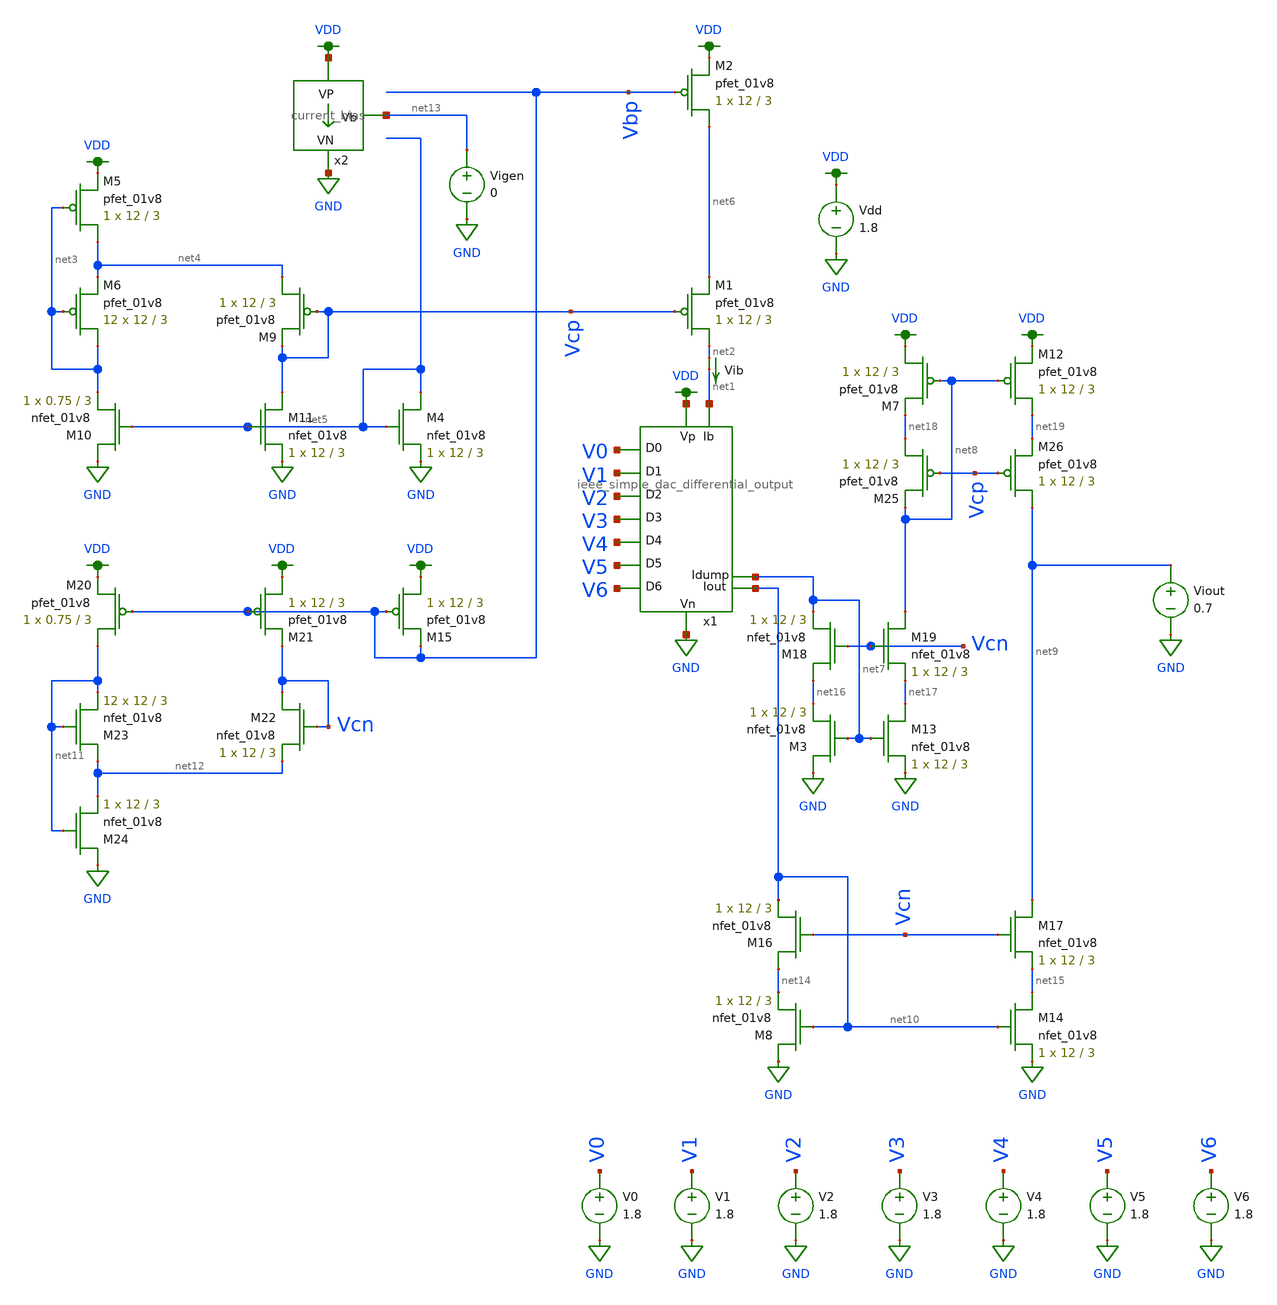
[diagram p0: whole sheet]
** sch_path: schematics/ieee DAC/ieee_DAC_mc_simulation_3.sch
**.subckt ieee_DAC_mc_simulation_3
Vdd VDD GND 1.8
V1 V1 GND 1.8
V2 V2 GND 1.8
V3 V3 GND 1.8
V4 V4 GND 1.8
V5 V5 GND 1.8
V6 V6 GND 1.8
V0 V0 GND 1.8
Vib net2 net1 0
.save i(vib)
XM1 net2 Vcp net6 VDD sky130_fd_pr__pfet_01v8 L=3 W=12 nf=1 ad='int((nf+1)/2) * W/nf * 0.29' as='int((nf+2)/2) * W/nf * 0.29'
+ pd='2*int((nf+1)/2) * (W/nf + 0.29)' ps='2*int((nf+2)/2) * (W/nf + 0.29)' nrd='0.29 / W' nrs='0.29 / W'
+ sa=0 sb=0 sd=0 mult=1 m=1
XM5 net4 net3 VDD VDD sky130_fd_pr__pfet_01v8 L=3 W=12 nf=1 ad='int((nf+1)/2) * W/nf * 0.29' as='int((nf+2)/2) * W/nf * 0.29'
+ pd='2*int((nf+1)/2) * (W/nf + 0.29)' ps='2*int((nf+2)/2) * (W/nf + 0.29)' nrd='0.29 / W' nrs='0.29 / W'
+ sa=0 sb=0 sd=0 mult=1 m=1
XM6 net3 net3 net4 VDD sky130_fd_pr__pfet_01v8 L=3 W=12 nf=1 ad='int((nf+1)/2) * W/nf * 0.29' as='int((nf+2)/2) * W/nf * 0.29'
+ pd='2*int((nf+1)/2) * (W/nf + 0.29)' ps='2*int((nf+2)/2) * (W/nf + 0.29)' nrd='0.29 / W' nrs='0.29 / W'
+ sa=0 sb=0 sd=0 mult=12 m=12
XM9 net4 Vcp Vcp VDD sky130_fd_pr__pfet_01v8 L=3 W=12 nf=1 ad='int((nf+1)/2) * W/nf * 0.29' as='int((nf+2)/2) * W/nf * 0.29'
+ pd='2*int((nf+1)/2) * (W/nf + 0.29)' ps='2*int((nf+2)/2) * (W/nf + 0.29)' nrd='0.29 / W' nrs='0.29 / W'
+ sa=0 sb=0 sd=0 mult=1 m=1
XM10 GND net5 net3 GND sky130_fd_pr__nfet_01v8 L=3 W=0.75 nf=1 ad='int((nf+1)/2) * W/nf * 0.29' as='int((nf+2)/2) * W/nf * 0.29'
+ pd='2*int((nf+1)/2) * (W/nf + 0.29)' ps='2*int((nf+2)/2) * (W/nf + 0.29)' nrd='0.29 / W' nrs='0.29 / W'
+ sa=0 sb=0 sd=0 mult=1 m=1
XM11 Vcp net5 GND GND sky130_fd_pr__nfet_01v8 L=3 W=12 nf=1 ad='int((nf+1)/2) * W/nf * 0.29' as='int((nf+2)/2) * W/nf * 0.29'
+ pd='2*int((nf+1)/2) * (W/nf + 0.29)' ps='2*int((nf+2)/2) * (W/nf + 0.29)' nrd='0.29 / W' nrs='0.29 / W'
+ sa=0 sb=0 sd=0 mult=1 m=1
XM2 net6 Vbp VDD VDD sky130_fd_pr__pfet_01v8 L=3 W=12 nf=1 ad='int((nf+1)/2) * W/nf * 0.29' as='int((nf+2)/2) * W/nf * 0.29'
+ pd='2*int((nf+1)/2) * (W/nf + 0.29)' ps='2*int((nf+2)/2) * (W/nf + 0.29)' nrd='0.29 / W' nrs='0.29 / W'
+ sa=0 sb=0 sd=0 mult=1 m=1
XM4 net5 net5 GND GND sky130_fd_pr__nfet_01v8 L=3 W=12 nf=1 ad='int((nf+1)/2) * W/nf * 0.29' as='int((nf+2)/2) * W/nf * 0.29'
+ pd='2*int((nf+1)/2) * (W/nf + 0.29)' ps='2*int((nf+2)/2) * (W/nf + 0.29)' nrd='0.29 / W' nrs='0.29 / W'
+ sa=0 sb=0 sd=0 mult=1 m=1
x2 VDD net13 GND current_bias
Vigen net13 GND 0
x1 VDD net7 GND V1 V0 V2 V3 V4 V5 V6 net1 net10 ieee_simple_dac_differential_output
XM3 GND net7 net16 GND sky130_fd_pr__nfet_01v8 L=3 W=12 nf=1 ad='int((nf+1)/2) * W/nf * 0.29' as='int((nf+2)/2) * W/nf * 0.29'
+ pd='2*int((nf+1)/2) * (W/nf + 0.29)' ps='2*int((nf+2)/2) * (W/nf + 0.29)' nrd='0.29 / W' nrs='0.29 / W'
+ sa=0 sb=0 sd=0 mult=1 m=1
XM7 VDD net8 net18 VDD sky130_fd_pr__pfet_01v8 L=3 W=12 nf=1 ad='int((nf+1)/2) * W/nf * 0.29' as='int((nf+2)/2) * W/nf * 0.29'
+ pd='2*int((nf+1)/2) * (W/nf + 0.29)' ps='2*int((nf+2)/2) * (W/nf + 0.29)' nrd='0.29 / W' nrs='0.29 / W'
+ sa=0 sb=0 sd=0 mult=1 m=1
XM8 GND net10 net14 GND sky130_fd_pr__nfet_01v8 L=3 W=12 nf=1 ad='int((nf+1)/2) * W/nf * 0.29' as='int((nf+2)/2) * W/nf * 0.29'
+ pd='2*int((nf+1)/2) * (W/nf + 0.29)' ps='2*int((nf+2)/2) * (W/nf + 0.29)' nrd='0.29 / W' nrs='0.29 / W'
+ sa=0 sb=0 sd=0 mult=1 m=1
XM12 net19 net8 VDD VDD sky130_fd_pr__pfet_01v8 L=3 W=12 nf=1 ad='int((nf+1)/2) * W/nf * 0.29' as='int((nf+2)/2) * W/nf * 0.29'
+ pd='2*int((nf+1)/2) * (W/nf + 0.29)' ps='2*int((nf+2)/2) * (W/nf + 0.29)' nrd='0.29 / W' nrs='0.29 / W'
+ sa=0 sb=0 sd=0 mult=1 m=1
Viout net9 GND 0.7
XM13 net17 net7 GND GND sky130_fd_pr__nfet_01v8 L=3 W=12 nf=1 ad='int((nf+1)/2) * W/nf * 0.29' as='int((nf+2)/2) * W/nf * 0.29'
+ pd='2*int((nf+1)/2) * (W/nf + 0.29)' ps='2*int((nf+2)/2) * (W/nf + 0.29)' nrd='0.29 / W' nrs='0.29 / W'
+ sa=0 sb=0 sd=0 mult=1 m=1
XM14 net15 net10 GND GND sky130_fd_pr__nfet_01v8 L=3 W=12 nf=1 ad='int((nf+1)/2) * W/nf * 0.29' as='int((nf+2)/2) * W/nf * 0.29'
+ pd='2*int((nf+1)/2) * (W/nf + 0.29)' ps='2*int((nf+2)/2) * (W/nf + 0.29)' nrd='0.29 / W' nrs='0.29 / W'
+ sa=0 sb=0 sd=0 mult=1 m=1
XM20 net11 Vbp VDD VDD sky130_fd_pr__pfet_01v8 L=3 W=0.75 nf=1 ad='int((nf+1)/2) * W/nf * 0.29' as='int((nf+2)/2) * W/nf * 0.29'
+ pd='2*int((nf+1)/2) * (W/nf + 0.29)' ps='2*int((nf+2)/2) * (W/nf + 0.29)' nrd='0.29 / W' nrs='0.29 / W'
+ sa=0 sb=0 sd=0 mult=1 m=1
XM21 VDD Vbp Vcn VDD sky130_fd_pr__pfet_01v8 L=3 W=12 nf=1 ad='int((nf+1)/2) * W/nf * 0.29' as='int((nf+2)/2) * W/nf * 0.29'
+ pd='2*int((nf+1)/2) * (W/nf + 0.29)' ps='2*int((nf+2)/2) * (W/nf + 0.29)' nrd='0.29 / W' nrs='0.29 / W'
+ sa=0 sb=0 sd=0 mult=1 m=1
XM22 Vcn Vcn net12 GND sky130_fd_pr__nfet_01v8 L=3 W=12 nf=1 ad='int((nf+1)/2) * W/nf * 0.29' as='int((nf+2)/2) * W/nf * 0.29'
+ pd='2*int((nf+1)/2) * (W/nf + 0.29)' ps='2*int((nf+2)/2) * (W/nf + 0.29)' nrd='0.29 / W' nrs='0.29 / W'
+ sa=0 sb=0 sd=0 mult=1 m=1
XM23 net12 net11 net11 GND sky130_fd_pr__nfet_01v8 L=3 W=12 nf=1 ad='int((nf+1)/2) * W/nf * 0.29' as='int((nf+2)/2) * W/nf * 0.29'
+ pd='2*int((nf+1)/2) * (W/nf + 0.29)' ps='2*int((nf+2)/2) * (W/nf + 0.29)' nrd='0.29 / W' nrs='0.29 / W'
+ sa=0 sb=0 sd=0 mult=12 m=12
XM24 GND net11 net12 GND sky130_fd_pr__nfet_01v8 L=3 W=12 nf=1 ad='int((nf+1)/2) * W/nf * 0.29' as='int((nf+2)/2) * W/nf * 0.29'
+ pd='2*int((nf+1)/2) * (W/nf + 0.29)' ps='2*int((nf+2)/2) * (W/nf + 0.29)' nrd='0.29 / W' nrs='0.29 / W'
+ sa=0 sb=0 sd=0 mult=1 m=1
XM15 VDD Vbp Vbp VDD sky130_fd_pr__pfet_01v8 L=3 W=12 nf=1 ad='int((nf+1)/2) * W/nf * 0.29' as='int((nf+2)/2) * W/nf * 0.29'
+ pd='2*int((nf+1)/2) * (W/nf + 0.29)' ps='2*int((nf+2)/2) * (W/nf + 0.29)' nrd='0.29 / W' nrs='0.29 / W'
+ sa=0 sb=0 sd=0 mult=1 m=1
XM16 net14 Vcn net10 GND sky130_fd_pr__nfet_01v8 L=3 W=12 nf=1 ad='int((nf+1)/2) * W/nf * 0.29' as='int((nf+2)/2) * W/nf * 0.29'
+ pd='2*int((nf+1)/2) * (W/nf + 0.29)' ps='2*int((nf+2)/2) * (W/nf + 0.29)' nrd='0.29 / W' nrs='0.29 / W'
+ sa=0 sb=0 sd=0 mult=1 m=1
XM17 net9 Vcn net15 GND sky130_fd_pr__nfet_01v8 L=3 W=12 nf=1 ad='int((nf+1)/2) * W/nf * 0.29' as='int((nf+2)/2) * W/nf * 0.29'
+ pd='2*int((nf+1)/2) * (W/nf + 0.29)' ps='2*int((nf+2)/2) * (W/nf + 0.29)' nrd='0.29 / W' nrs='0.29 / W'
+ sa=0 sb=0 sd=0 mult=1 m=1
XM18 net16 Vcn net7 GND sky130_fd_pr__nfet_01v8 L=3 W=12 nf=1 ad='int((nf+1)/2) * W/nf * 0.29' as='int((nf+2)/2) * W/nf * 0.29'
+ pd='2*int((nf+1)/2) * (W/nf + 0.29)' ps='2*int((nf+2)/2) * (W/nf + 0.29)' nrd='0.29 / W' nrs='0.29 / W'
+ sa=0 sb=0 sd=0 mult=1 m=1
XM19 net8 Vcn net17 GND sky130_fd_pr__nfet_01v8 L=3 W=12 nf=1 ad='int((nf+1)/2) * W/nf * 0.29' as='int((nf+2)/2) * W/nf * 0.29'
+ pd='2*int((nf+1)/2) * (W/nf + 0.29)' ps='2*int((nf+2)/2) * (W/nf + 0.29)' nrd='0.29 / W' nrs='0.29 / W'
+ sa=0 sb=0 sd=0 mult=1 m=1
XM25 net18 Vcp net8 VDD sky130_fd_pr__pfet_01v8 L=3 W=12 nf=1 ad='int((nf+1)/2) * W/nf * 0.29' as='int((nf+2)/2) * W/nf * 0.29'
+ pd='2*int((nf+1)/2) * (W/nf + 0.29)' ps='2*int((nf+2)/2) * (W/nf + 0.29)' nrd='0.29 / W' nrs='0.29 / W'
+ sa=0 sb=0 sd=0 mult=1 m=1
XM26 net9 Vcp net19 VDD sky130_fd_pr__pfet_01v8 L=3 W=12 nf=1 ad='int((nf+1)/2) * W/nf * 0.29' as='int((nf+2)/2) * W/nf * 0.29'
+ pd='2*int((nf+1)/2) * (W/nf + 0.29)' ps='2*int((nf+2)/2) * (W/nf + 0.29)' nrd='0.29 / W' nrs='0.29 / W'
+ sa=0 sb=0 sd=0 mult=1 m=1
**** begin user architecture code

.option wnflag=1
.param MC_SWITCH=1.0
.lib ~/skywater/skywater-pdk/libraries/sky130_fd_pr_ngspice/latest/models/sky130.lib.spice tt


.save all
.control
set wr_vecnames
set wr_singlescale

let Ibias_max = 31n
let Ibias = 30n
dowhile Ibias < Ibias_max
alter Ib $&Ibias

let mc_runs = 10
let run = 1
dowhile run <= mc_runs

  let code = 0
  while code < 128
    if floor(code / 1) eq 0
      let b0 = 0
    else
      let b0 = (floor(code / 1) % 2) * 1.8
    end
    if floor(code / 2) eq 0
      let b1 = 0
    else
      let b1 = (floor(code / 2) % 2) * 1.8
    end
    if floor(code / 4) eq 0
      let b2 = 0
    else
      let b2 = (floor(code / 4) % 2) * 1.8
    end
    if floor(code / 8) eq 0
      let b3 = 0
    else
      let b3 = (floor(code / 8) % 2) * 1.8
    end
    if floor(code / 16) eq 0
      let b4 = 0
    else
      let b4 = (floor(code / 16) % 2) * 1.8
    end
    if floor(code / 32) eq 0
      let b5 = 0
    else
      let b5 = (floor(code / 32) % 2) * 1.8
    end
    if floor(code / 64) eq 0
      let b6 = 0
    else
      let b6 = (floor(code / 64) % 2) * 1.8
    end

    alter V0 $&b0
    alter V1 $&b1
    alter V2 $&b2
    alter V3 $&b3
    alter V4 $&b4
    alter V5 $&b5
    alter V6 $&b6
    save all
    op

    wrdata ~/dev/git/7-bit-D-A-converter-MP4-MADVLSI/schematics/simulations/ieee_DAC/dac_with_external_bias_gen/test_10/ieeeDAC_{$&run}.txt
+ V0 V1 V2 V3 V4 V5 V6 i(Vib) i(Viout)
    if code eq 0
      set appendwrite
      set wr_vecnames = FALSE
    end
    let code = code + 1
  end
  reset
  set appendwrite = FALSE
  set wr_vecnames
  let run = run + 1
end

let Ibias = Ibias * 2
end
.endc

**** end user architecture code
**.ends
.GLOBAL VDD
.GLOBAL GND
.end
